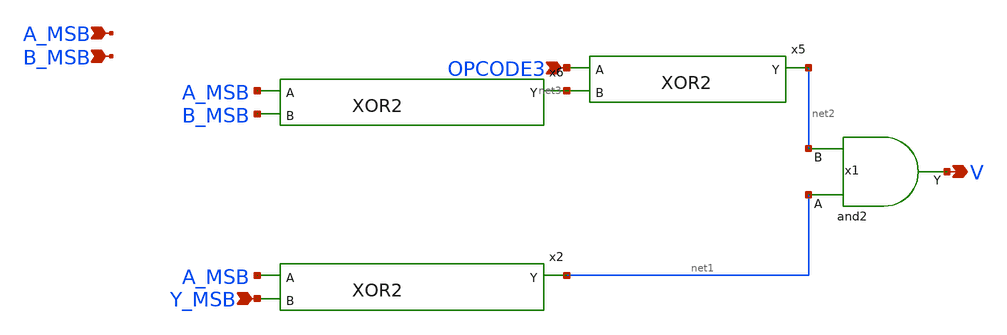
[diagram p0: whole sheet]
** sch_path: design/xschem/ZV_FLAG/V_FLAG.sch
**.subckt V_FLAG V A_MSB B_MSB OPCODE3 Y_MSB
*.opin V
*.ipin A_MSB
*.ipin B_MSB
*.ipin OPCODE3
*.ipin Y_MSB
x5 OPCODE3 net3 net2 VSS VDD XOR2
x6 A_MSB B_MSB net3 VSS VDD XOR2
x2 A_MSB Y_MSB net1 VSS VDD XOR2
x1 net1 net2 VSS VDD V and2
**.ends
.end
